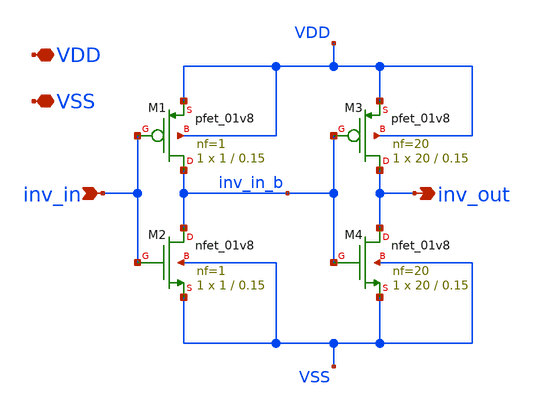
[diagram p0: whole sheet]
** sch_path: xschem/double_inverter.sch
**.subckt double_inverter VDD VSS inv_in inv_out
*.iopin VDD
*.iopin VSS
*.ipin inv_in
*.opin inv_out
XM1 inv_in_b inv_in VDD VDD sky130_fd_pr__pfet_01v8 L=0.15 W=1 nf=1 ad='int((nf+1)/2) * W/nf * 0.29'
+ as='int((nf+2)/2) * W/nf * 0.29' pd='2*int((nf+1)/2) * (W/nf + 0.29)' ps='2*int((nf+2)/2) * (W/nf + 0.29)'
+ nrd='0.29 / W' nrs='0.29 / W' sa=0 sb=0 sd=0 mult=1 m=1
XM2 inv_in_b inv_in VSS VSS sky130_fd_pr__nfet_01v8 L=0.15 W=1 nf=1 ad='int((nf+1)/2) * W/nf * 0.29'
+ as='int((nf+2)/2) * W/nf * 0.29' pd='2*int((nf+1)/2) * (W/nf + 0.29)' ps='2*int((nf+2)/2) * (W/nf + 0.29)'
+ nrd='0.29 / W' nrs='0.29 / W' sa=0 sb=0 sd=0 mult=1 m=1
XM3 inv_out inv_in_b VDD VDD sky130_fd_pr__pfet_01v8 L=0.15 W=20 nf=20 ad='int((nf+1)/2) * W/nf * 0.29'
+ as='int((nf+2)/2) * W/nf * 0.29' pd='2*int((nf+1)/2) * (W/nf + 0.29)' ps='2*int((nf+2)/2) * (W/nf + 0.29)'
+ nrd='0.29 / W' nrs='0.29 / W' sa=0 sb=0 sd=0 mult=1 m=1
XM4 inv_out inv_in_b VSS VSS sky130_fd_pr__nfet_01v8 L=0.15 W=20 nf=20 ad='int((nf+1)/2) * W/nf * 0.29'
+ as='int((nf+2)/2) * W/nf * 0.29' pd='2*int((nf+1)/2) * (W/nf + 0.29)' ps='2*int((nf+2)/2) * (W/nf + 0.29)'
+ nrd='0.29 / W' nrs='0.29 / W' sa=0 sb=0 sd=0 mult=1 m=1
**.ends
.end
